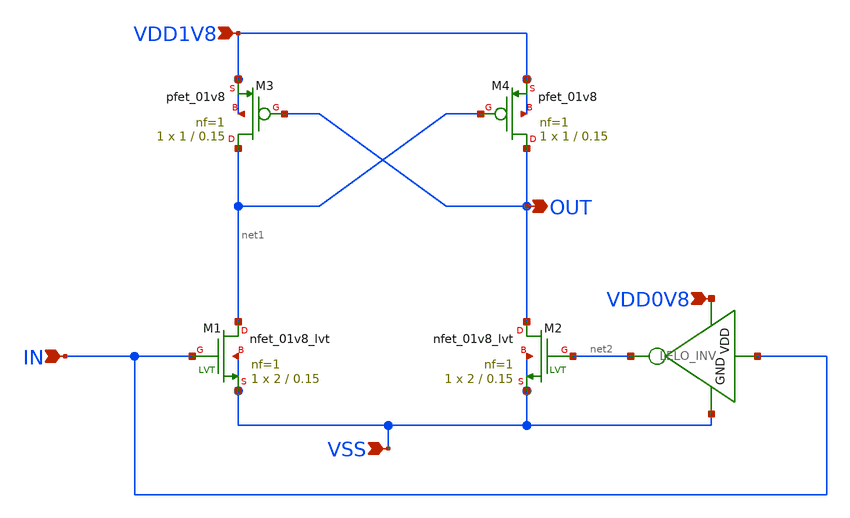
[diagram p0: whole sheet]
** sch_path: design/LELO_SVOD_SKY130A/LELO_SVOD_LEVELSHIFT.sch
**.subckt LELO_SVOD_LEVELSHIFT VDD1V8 VDD0V8 IN VSS OUT
*.ipin VDD1V8
*.ipin VDD0V8
*.ipin IN
*.ipin VSS
*.opin OUT
XM1 net1 IN VSS VSS sky130_fd_pr__nfet_01v8_lvt L=0.15 W=2 nf=1 ad='int((1 + 1)/2) * 2 / 1 * 0.29' as='int((1 + 2)/2) * 2 / 1 * 0.29'
+ pd='2*int((1 + 1)/2) * (2 / 1 + 0.29)' ps='2*int((1 + 2)/2) * (2 / 1 + 0.29)' nrd='0.29 / 2 ' nrs='0.29 / 2 '
+ sa=0 sb=0 sd=0 mult=1 m=1
XM2 OUT net2 VSS VSS sky130_fd_pr__nfet_01v8_lvt L=0.15 W=2 nf=1 ad='int((1 + 1)/2) * 2 / 1 * 0.29' as='int((1 + 2)/2) * 2 / 1 * 0.29'
+ pd='2*int((1 + 1)/2) * (2 / 1 + 0.29)' ps='2*int((1 + 2)/2) * (2 / 1 + 0.29)' nrd='0.29 / 2 ' nrs='0.29 / 2 '
+ sa=0 sb=0 sd=0 mult=1 m=1
x1 VDD0V8 IN net2 VSS LELO_INV
XM3 net1 OUT VDD1V8 VDD1V8 sky130_fd_pr__pfet_01v8 L=0.15 W=1 nf=1 ad='int((1 + 1)/2) * 1 / 1 * 0.29'
+ as='int((1 + 2)/2) * 1 / 1 * 0.29' pd='2*int((1 + 1)/2) * (1 / 1 + 0.29)' ps='2*int((1 + 2)/2) * (1 / 1 + 0.29)'
+ nrd='0.29 / 1 ' nrs='0.29 / 1 ' sa=0 sb=0 sd=0 mult=1 m=1
XM4 OUT net1 VDD1V8 VDD1V8 sky130_fd_pr__pfet_01v8 L=0.15 W=1 nf=1 ad='int((1 + 1)/2) * 1 / 1 * 0.29'
+ as='int((1 + 2)/2) * 1 / 1 * 0.29' pd='2*int((1 + 1)/2) * (1 / 1 + 0.29)' ps='2*int((1 + 2)/2) * (1 / 1 + 0.29)'
+ nrd='0.29 / 1 ' nrs='0.29 / 1 ' sa=0 sb=0 sd=0 mult=1 m=1
**.ends

* expanding   symbol:  LELO_SVOD_SKY130A/LELO_INV.sym # of pins=4
** sym_path: design/LELO_SVOD_SKY130A/LELO_INV.sym
** sch_path: design/LELO_SVOD_SKY130A/LELO_INV.sch
.subckt LELO_INV VDD VIN VOUT GND
*.ipin VIN
*.ipin VDD
*.ipin GND
*.opin VOUT
XM1 VOUT VIN GND GND sky130_fd_pr__nfet_01v8_lvt L=0.15 W=1 nf=1 ad='int((1 + 1)/2) * 1 / 1 * 0.29' as='int((1 + 2)/2) * 1 / 1 * 0.29'
+ pd='2*int((1 + 1)/2) * (1 / 1 + 0.29)' ps='2*int((1 + 2)/2) * (1 / 1 + 0.29)' nrd='0.29 / 1 ' nrs='0.29 / 1 '
+ sa=0 sb=0 sd=0 mult=1 m=1
XM2 VOUT VIN VDD VDD sky130_fd_pr__pfet_01v8_lvt L=0.35 W=1 nf=1 ad='int((1 + 1)/2) * 1 / 1 * 0.29' as='int((1 + 2)/2) * 1 / 1 * 0.29'
+ pd='2*int((1 + 1)/2) * (1 / 1 + 0.29)' ps='2*int((1 + 2)/2) * (1 / 1 + 0.29)' nrd='0.29 / 1 ' nrs='0.29 / 1 '
+ sa=0 sb=0 sd=0 mult=2 m=2
.ends

.end
